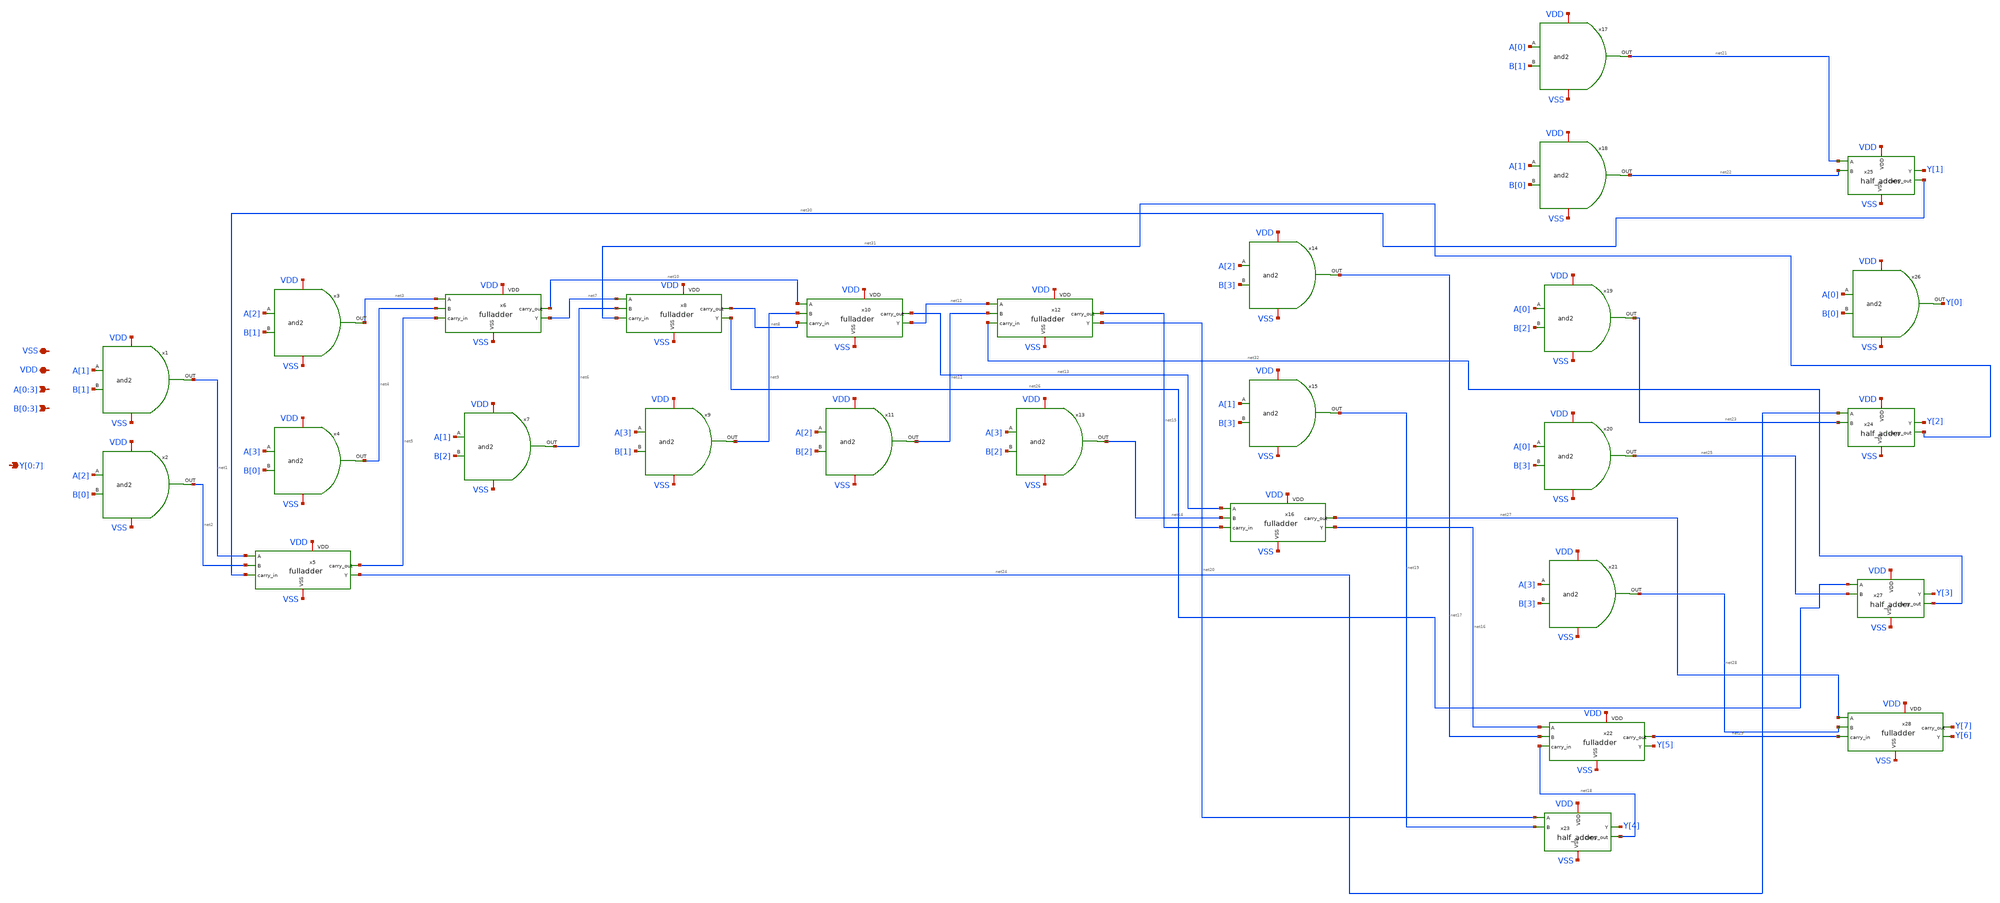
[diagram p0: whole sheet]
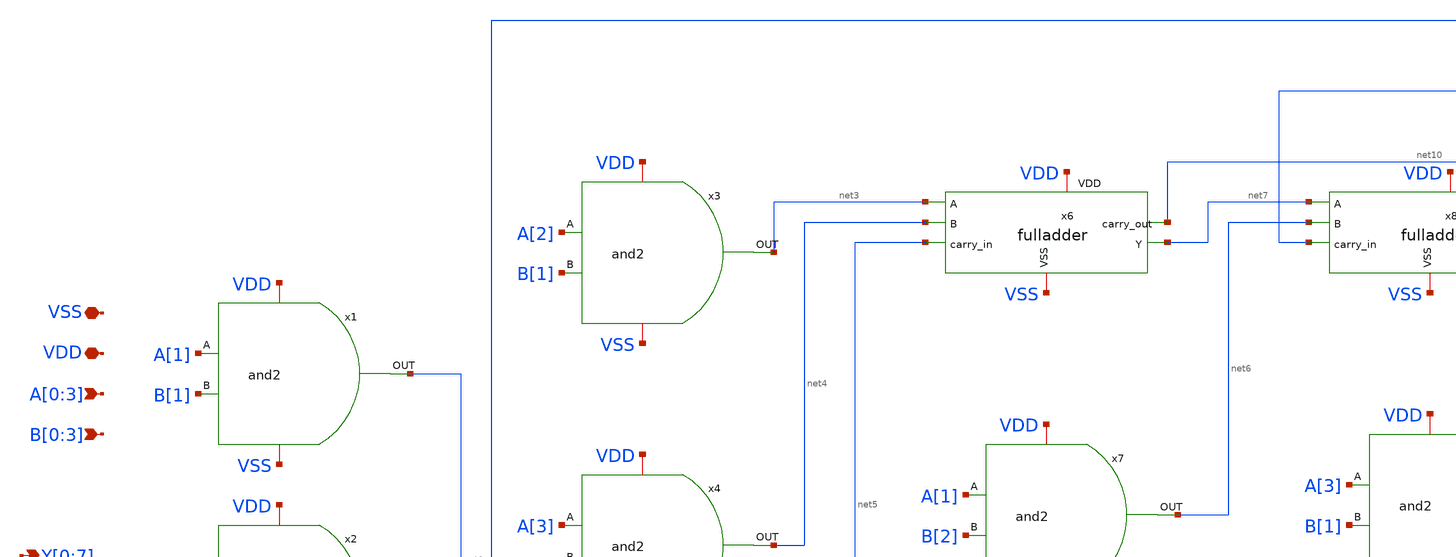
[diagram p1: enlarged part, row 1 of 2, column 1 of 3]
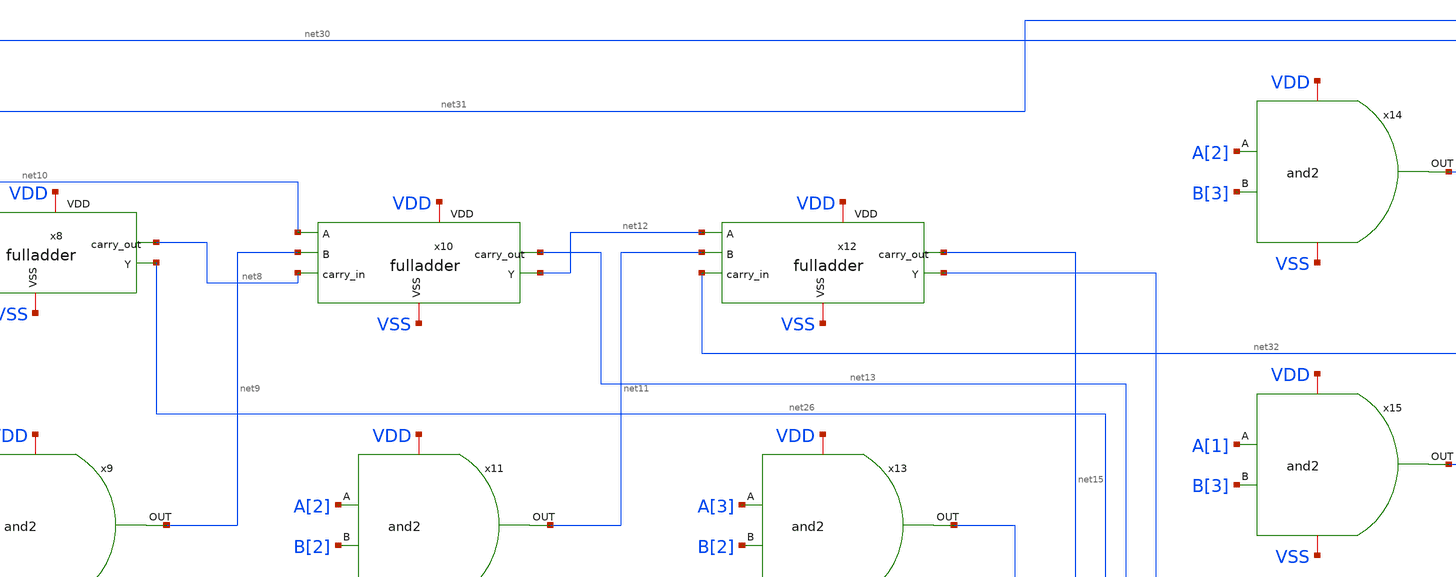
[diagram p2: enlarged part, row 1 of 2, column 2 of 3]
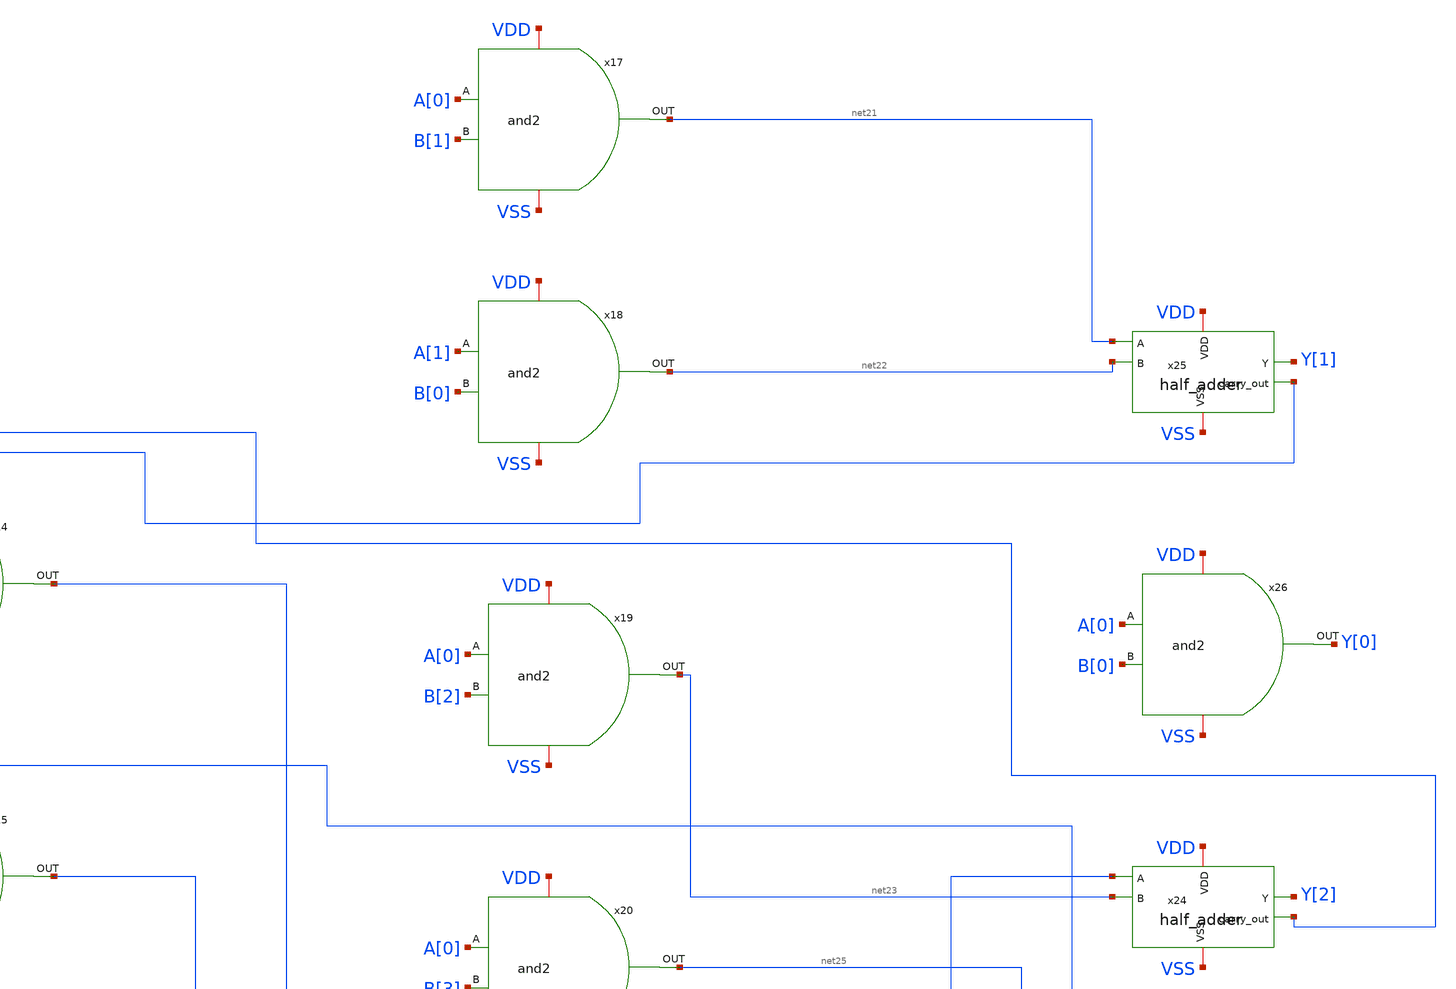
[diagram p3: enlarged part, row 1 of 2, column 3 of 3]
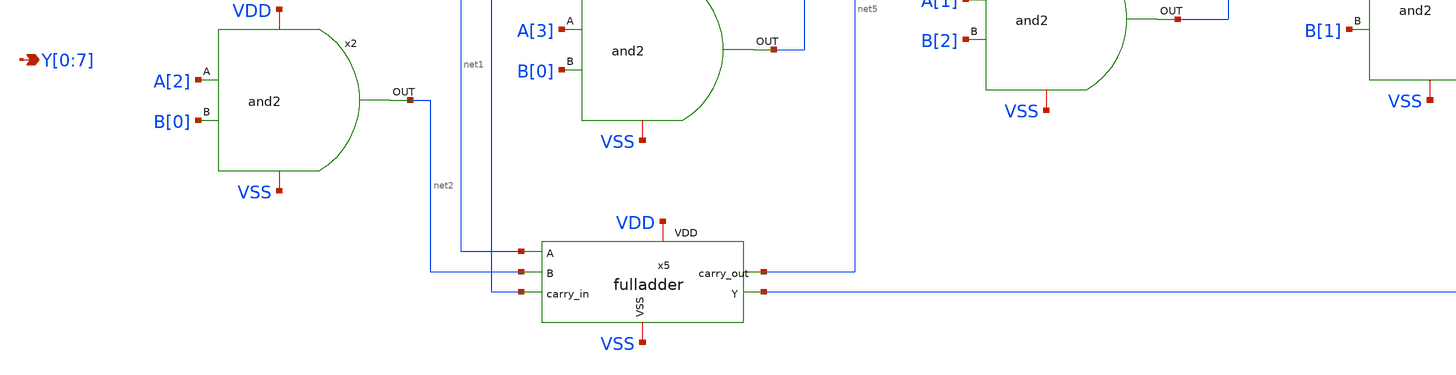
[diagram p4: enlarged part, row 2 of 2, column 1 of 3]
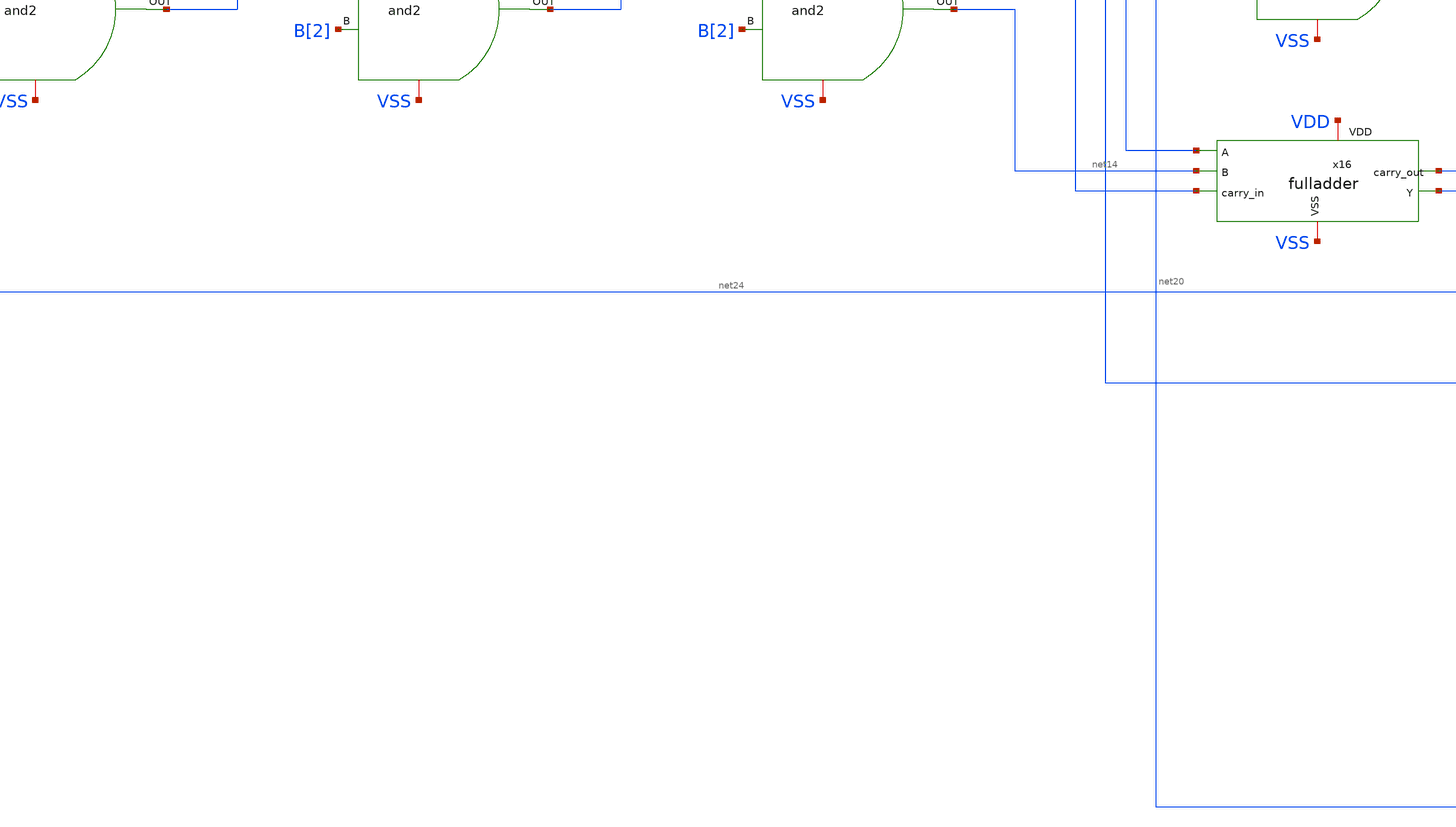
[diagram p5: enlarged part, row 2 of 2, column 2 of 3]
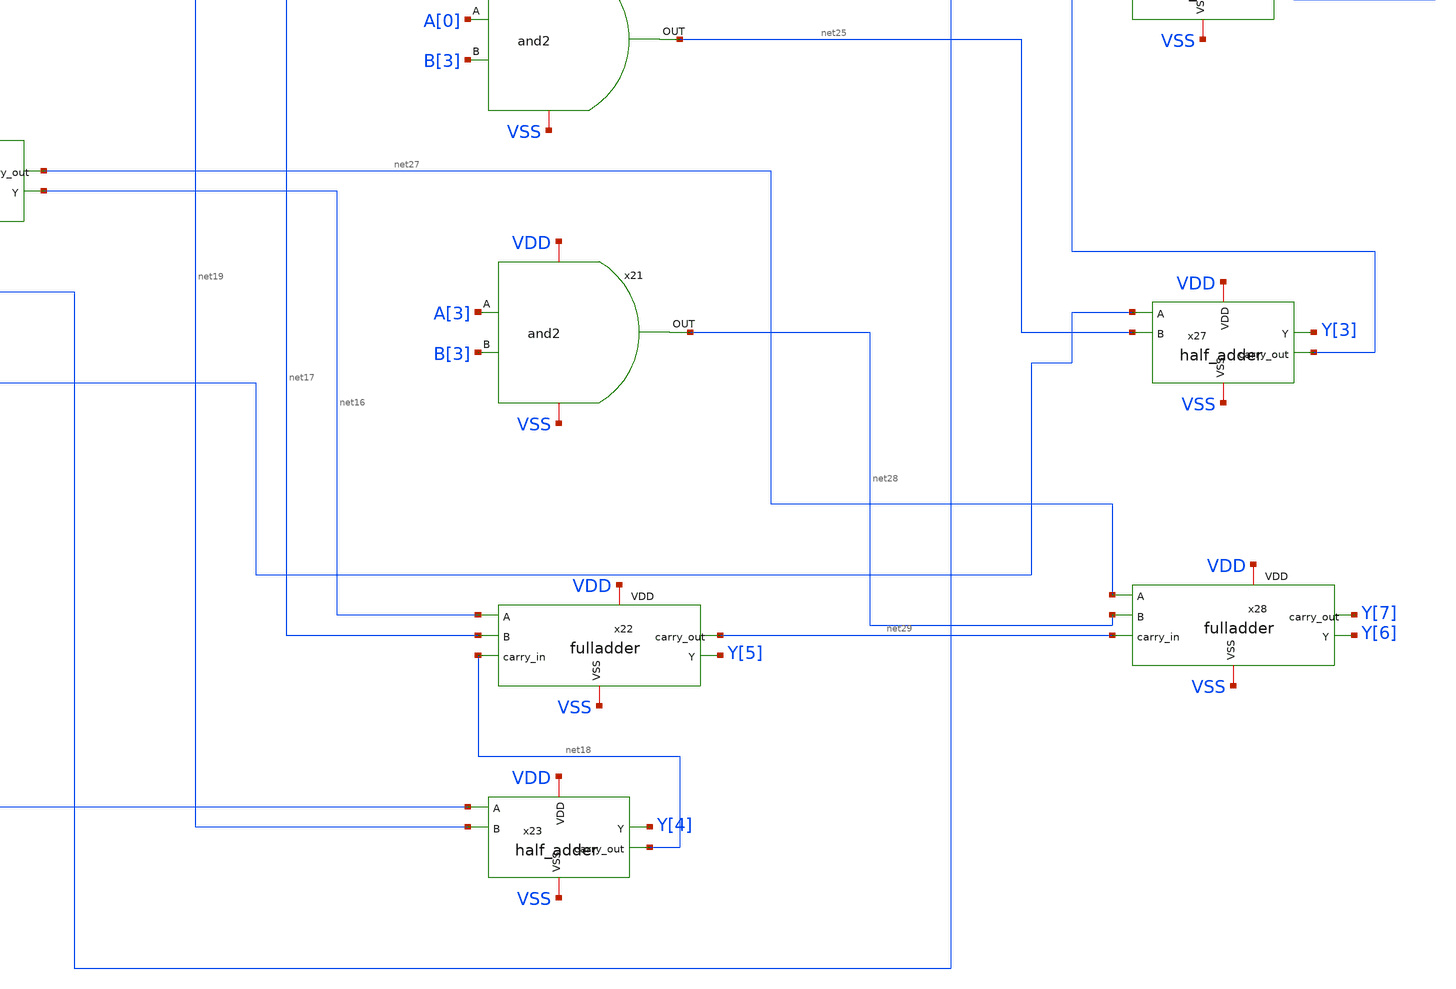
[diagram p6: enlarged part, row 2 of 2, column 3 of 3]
** sch_path: design/ALU/array_multiplier.sch
**.subckt array_multiplier A[0],A[1],A[2],A[3] B[0],B[1],B[2],B[3] VDD VSS
*+ Y[0],Y[1],Y[2],Y[3],Y[4],Y[5],Y[6],Y[7]
*.ipin A[0],A[1],A[2],A[3]
*.ipin B[0],B[1],B[2],B[3]
*.iopin VDD
*.iopin VSS
*.opin Y[0],Y[1],Y[2],Y[3],Y[4],Y[5],Y[6],Y[7]
x1 VSS A[1] B[1] VDD net1 and2
x2 VSS A[2] B[0] VDD net2 and2
x3 VSS A[2] B[1] VDD net3 and2
x4 VSS A[3] B[0] VDD net4 and2
x5 net1 net2 net30 VDD VSS net5 net24 fulladder
x6 net3 net4 net5 VDD VSS net10 net7 fulladder
x7 VSS A[1] B[2] VDD net6 and2
x8 net7 net6 net31 VDD VSS net8 net26 fulladder
x9 VSS A[3] B[1] VDD net9 and2
x10 net10 net9 net8 VDD VSS net13 net12 fulladder
x11 VSS A[2] B[2] VDD net11 and2
x12 net12 net11 net32 VDD VSS net15 net20 fulladder
x13 VSS A[3] B[2] VDD net14 and2
x14 VSS A[2] B[3] VDD net17 and2
x15 VSS A[1] B[3] VDD net19 and2
x17 VSS A[0] B[1] VDD net21 and2
x18 VSS A[1] B[0] VDD net22 and2
x19 VSS A[0] B[2] VDD net23 and2
x20 VSS A[0] B[3] VDD net25 and2
x21 VSS A[3] B[3] VDD net28 and2
x22 net16 net17 net18 VDD VSS net29 Y[5] fulladder
x23 net20 net19 Y[4] net18 VDD VSS half_adder
x16 net13 net14 net15 VDD VSS net27 net16 fulladder
x24 net24 net23 Y[2] net31 VDD VSS half_adder
x25 net21 net22 Y[1] net30 VDD VSS half_adder
x26 VSS A[0] B[0] VDD Y[0] and2
x27 net26 net25 Y[3] net32 VDD VSS half_adder
x28 net27 net28 net29 VDD VSS Y[7] Y[6] fulladder
**.ends
.end
